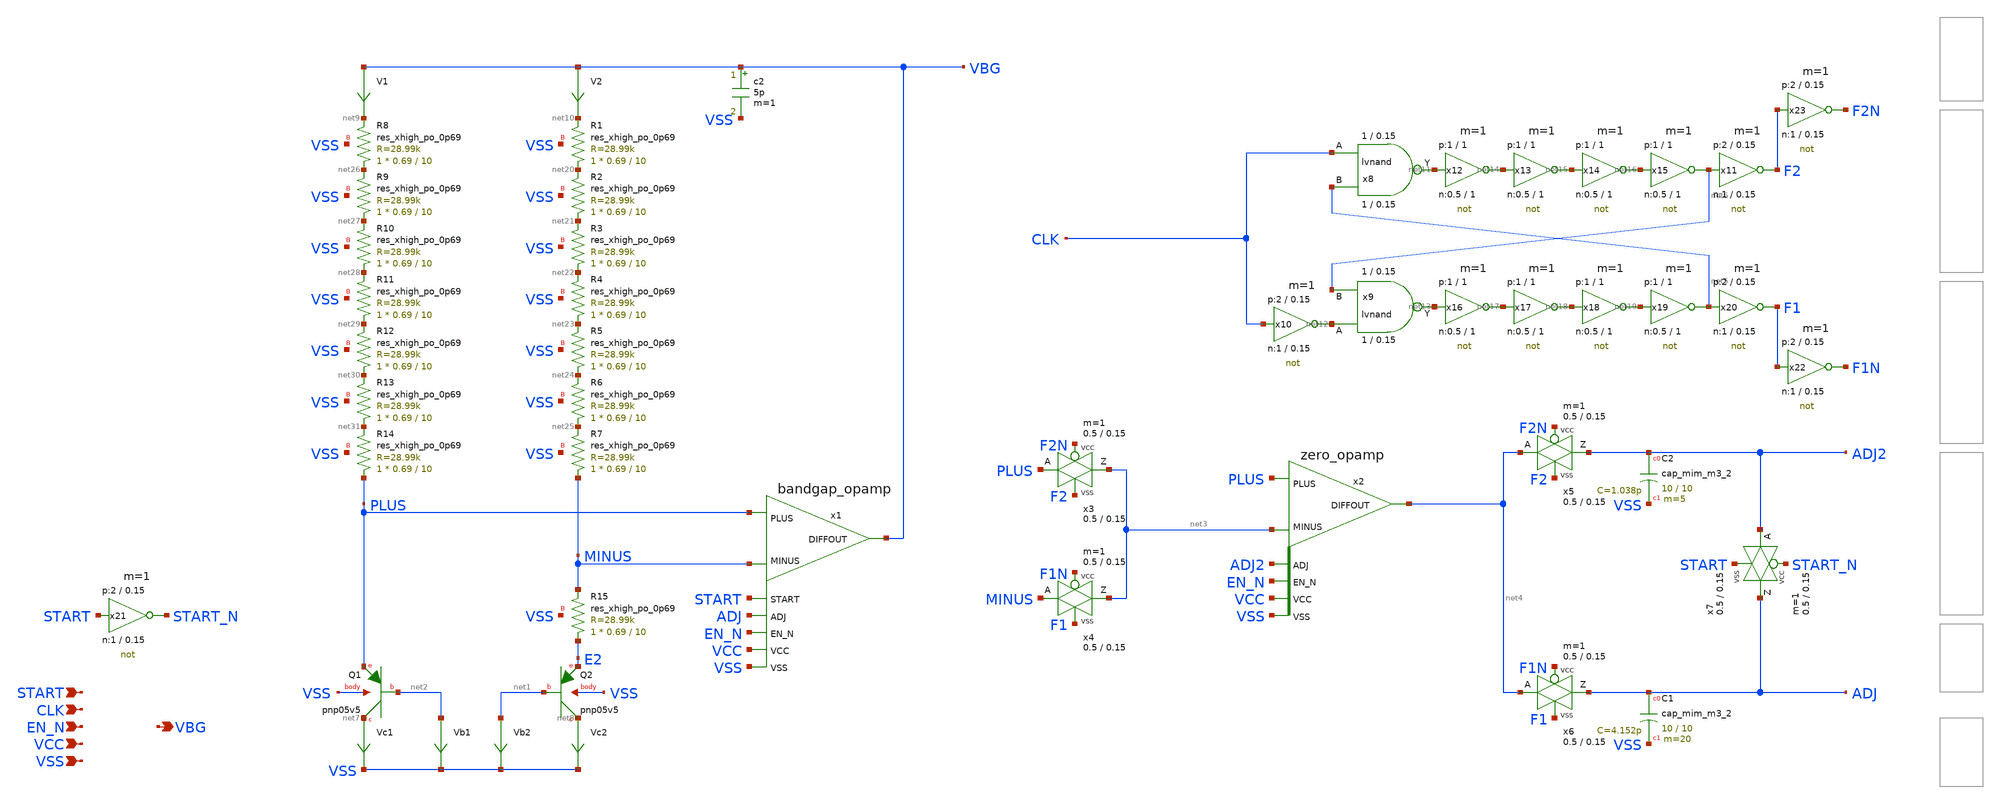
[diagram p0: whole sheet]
** sch_path: sky130_tests/bandgap.sch
* Copyright 2021 Stefan Frederik Schippers
* Licensed under the Apache License, Version 2.0 (the "License");
* you may not use this file except in compliance with the License.
* You may obtain a copy of the License at
* https://www.apache.org/licenses/LICENSE-2.0
* Unless required by applicable law or agreed to in writing, software
* distributed under the License is distributed on an "AS IS" BASIS,
* WITHOUT WARRANTIES OR CONDITIONS OF ANY KIND, either express or implied.
* See the License for the specific language governing permissions and
* limitations under the License.
**.subckt bandgap EN_N VBG VCC VSS CLK START
*.ipin EN_N
*.opin VBG
*.ipin VCC
*.ipin VSS
*.ipin CLK
*.ipin START
XQ1 net7 net2 PLUS VSS sky130_fd_pr__pnp_05v5_W0p68L0p68 m=1
XQ2 net8 net1 E2 VSS sky130_fd_pr__pnp_05v5_W0p68L0p68 m=8
Vc1 net7 VSS 0
.save i(vc1)
Vb1 net2 VSS 0
.save i(vb1)
Vb2 net1 VSS 0
.save i(vb2)
Vc2 net8 VSS 0
.save i(vc2)
x1 EN_N MINUS PLUS VBG VCC VSS ADJ START bandgap_opamp
V1 VBG net9 0
.save i(v1)
V2 VBG net10 0
.save i(v2)
x2 EN_N net3 PLUS net4 VCC VSS ADJ2 zero_opamp
x3 net3 PLUS F2N F2 VCC VSS passgate W_N=0.5 L_N=0.15 W_P=0.5 L_P=0.15 m=1
x4 net3 MINUS F1N F1 VCC VSS passgate W_N=0.5 L_N=0.15 W_P=0.5 L_P=0.15 m=1
x5 ADJ2 net4 F2N F2 VCC VSS passgate W_N=0.5 L_N=0.15 W_P=0.5 L_P=0.15 m=1
x6 ADJ net4 F1N F1 VCC VSS passgate W_N=0.5 L_N=0.15 W_P=0.5 L_P=0.15 m=1
x8 CLK net5 net11 lvnand WidthN=1 LenN=0.15 WidthP=1 LenP=0.15 m=1
x9 net12 net6 net13 lvnand WidthN=1 LenN=0.15 WidthP=1 LenP=0.15 m=1
x10 net12 CLK VCC VSS not W_N=1 L_N=0.15 W_P=2 L_P=0.15 m=1
x11 F2 net6 VCC VSS not W_N=1 L_N=0.15 W_P=2 L_P=0.15 m=1
x12 net14 net11 VCC VSS not W_N=0.5 L_N=1 W_P=1 L_P=1 m=1
x13 net15 net14 VCC VSS not W_N=0.5 L_N=1 W_P=1 L_P=1 m=1
x14 net16 net15 VCC VSS not W_N=0.5 L_N=1 W_P=1 L_P=1 m=1
x15 net6 net16 VCC VSS not W_N=0.5 L_N=1 W_P=1 L_P=1 m=1
x16 net17 net13 VCC VSS not W_N=0.5 L_N=1 W_P=1 L_P=1 m=1
x17 net18 net17 VCC VSS not W_N=0.5 L_N=1 W_P=1 L_P=1 m=1
x18 net19 net18 VCC VSS not W_N=0.5 L_N=1 W_P=1 L_P=1 m=1
x19 net5 net19 VCC VSS not W_N=0.5 L_N=1 W_P=1 L_P=1 m=1
x20 F1 net5 VCC VSS not W_N=1 L_N=0.15 W_P=2 L_P=0.15 m=1
c2 VBG VSS 5p m=1
x7 ADJ ADJ2 START_N START VCC VSS passgate W_N=0.5 L_N=0.15 W_P=0.5 L_P=0.15 m=1
x21 START_N START VCC VSS not W_N=1 L_N=0.15 W_P=2 L_P=0.15 m=1
x22 F1N F1 VCC VSS not W_N=1 L_N=0.15 W_P=2 L_P=0.15 m=1
x23 F2N F2 VCC VSS not W_N=1 L_N=0.15 W_P=2 L_P=0.15 m=1
XC2 ADJ2 VSS sky130_fd_pr__cap_mim_m3_2 W=10 L=10 MF=5 m=5
XC1 ADJ VSS sky130_fd_pr__cap_mim_m3_2 W=10 L=10 MF=20 m=20
XR1 net20 net10 VSS sky130_fd_pr__res_xhigh_po_0p69 L=10 mult=1 m=1
XR2 net21 net20 VSS sky130_fd_pr__res_xhigh_po_0p69 L=10 mult=1 m=1
XR3 net22 net21 VSS sky130_fd_pr__res_xhigh_po_0p69 L=10 mult=1 m=1
XR4 net23 net22 VSS sky130_fd_pr__res_xhigh_po_0p69 L=10 mult=1 m=1
XR5 net24 net23 VSS sky130_fd_pr__res_xhigh_po_0p69 L=10 mult=1 m=1
XR6 net25 net24 VSS sky130_fd_pr__res_xhigh_po_0p69 L=10 mult=1 m=1
XR7 MINUS net25 VSS sky130_fd_pr__res_xhigh_po_0p69 L=10 mult=1 m=1
XR8 net26 net9 VSS sky130_fd_pr__res_xhigh_po_0p69 L=10 mult=1 m=1
XR9 net27 net26 VSS sky130_fd_pr__res_xhigh_po_0p69 L=10 mult=1 m=1
XR10 net28 net27 VSS sky130_fd_pr__res_xhigh_po_0p69 L=10 mult=1 m=1
XR11 net29 net28 VSS sky130_fd_pr__res_xhigh_po_0p69 L=10 mult=1 m=1
XR12 net30 net29 VSS sky130_fd_pr__res_xhigh_po_0p69 L=10 mult=1 m=1
XR13 net31 net30 VSS sky130_fd_pr__res_xhigh_po_0p69 L=10 mult=1 m=1
XR14 PLUS net31 VSS sky130_fd_pr__res_xhigh_po_0p69 L=10 mult=1 m=1
XR15 E2 MINUS VSS sky130_fd_pr__res_xhigh_po_0p69 L=10 mult=1 m=1
**.ends
.end
